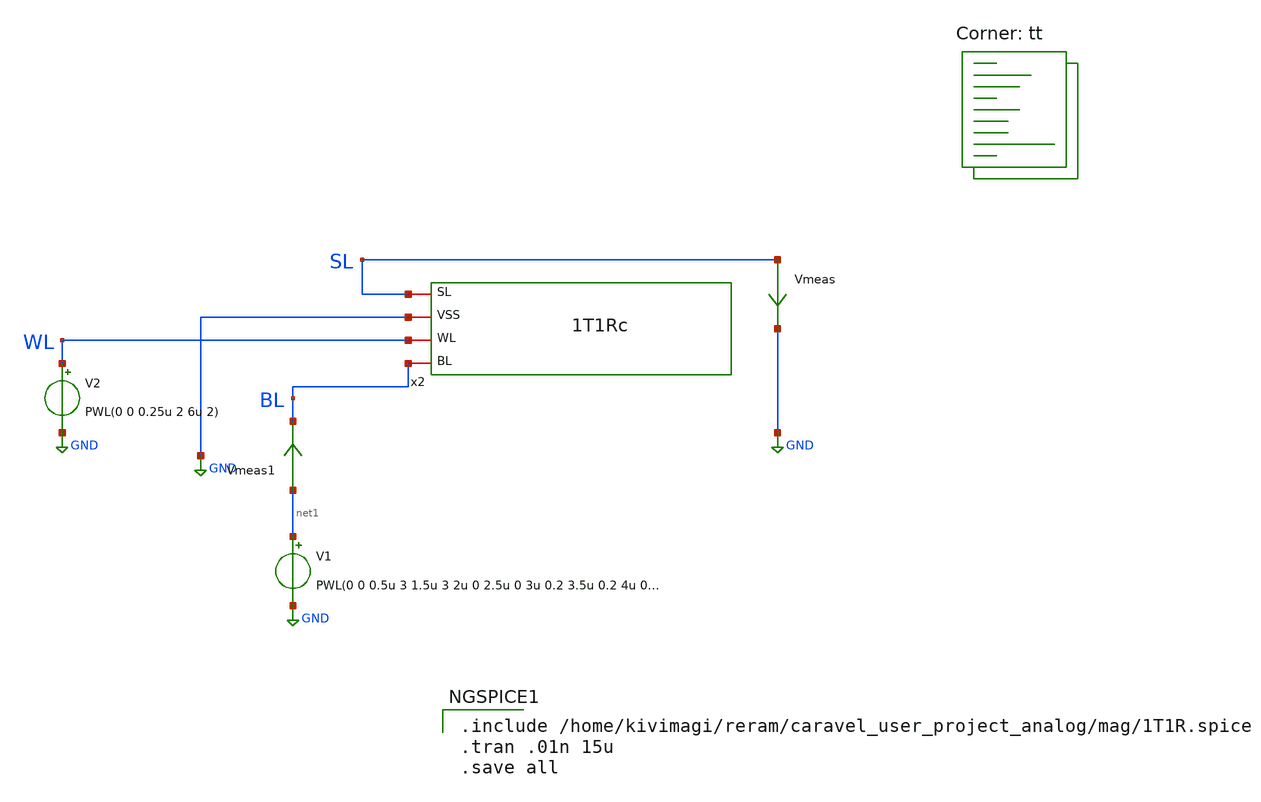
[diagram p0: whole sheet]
** sch_path: xschem/Crossbar/1t1rTBregular.sch
* StefanSchippers/xschem_sky130/sky130_fd_pr/reram.sym:
* Copyright 2021 Stefan Frederik Schippers
* Licensed under the Apache License, Version 2.0 (the "License");
**.subckt 1t1rTBregular
Vmeas SL GND 0
.save i(vmeas)
V2 WL GND PWL(0 0 0.25u 2 6u 2)
Vmeas1 net1 BL 0
.save i(vmeas1)
V1 net1 GND PWL(0 0 0.5u 3 1.5u 3 2u 0 2.5u 0 3u 0.2 3.5u 0.2 4u 0 4.5u -2.5 5.5u -2.5 6u 0 6.5u
+ 0.2)
x2 BL WL GND SL 1T1Rc
**** begin user architecture code
.lib $::SKYWATER_MODELS/sky130.lib.spice tt

.include /home/kivimagi/reram/caravel_user_project_analog/mag/1T1R.spice
.tran .01n 15u
.save all


**** end user architecture code
**.ends

* expanding   symbol:  Crossbar/1T1Rc.sym # of pins=4
** sym_path: xschem/1T1Rc.sym
** sch_path: xschem/1T1Rc.sch
.subckt 1T1Rc BL WL VSS SL
*.iopin SL
*.iopin VSS
*.iopin WL
*.iopin BL
XR1 BL net1 sky130_fd_pr_reram__reram_cell Tfilament_0=3.8e-9
XM1 net1 WL SL VSS sky130_fd_pr__nfet_g5v0d10v5 L=0.5 W=7 nf=1 ad='int((nf+1)/2) * W/nf * 0.29' as='int((nf+2)/2) * W/nf * 0.29'
+ pd='2*int((nf+1)/2) * (W/nf + 0.29)' ps='2*int((nf+2)/2) * (W/nf + 0.29)' nrd='0.29 / W' nrs='0.29 / W'
+ sa=0 sb=0 sd=0 mult=1 m=1
.ends

.GLOBAL GND
**** begin user architecture code

.subckt sky130_fd_pr_reram__reram_cell TE BE Tfilament_0=3.3e-9 area_ox=0.1024e-12
N1 TE BE nFilament sky130_fd_pr_reram__reram_model
.ic v(nFilament)={Tfilament_0*1.0e9}
.ends sky130_fd_pr_reram__reram_cell

.model sky130_fd_pr_reram__reram_model sky130_fd_pr_reram__reram_module  area_ox = 0.1024e-12  Tox =
+ 5.0  Tfilament_max = 4.9  Tfilament_min = 3.3  Eact_generation = 1.501  Eact_recombination  = 1.500
+  I_k1  = 6.140e-5  Tfilament_ref = 4.7249  V_ref = 0.430  velocity_k1 = 150  gamma_k0  = 16.5  gamma_k1
+  = -1.25  Temperature_0 = 300  C_thermal = 3.1825e-16  tau_thermal = 0.23e-9  t_step  = 1.0e-9
+  smoothing = 1e-7  Kclip = 200

.control
pre_osdi $SKYWATER_MODELS/sky130_fd_pr_reram__reram_module.osdi
.endc

**** end user architecture code
.end
